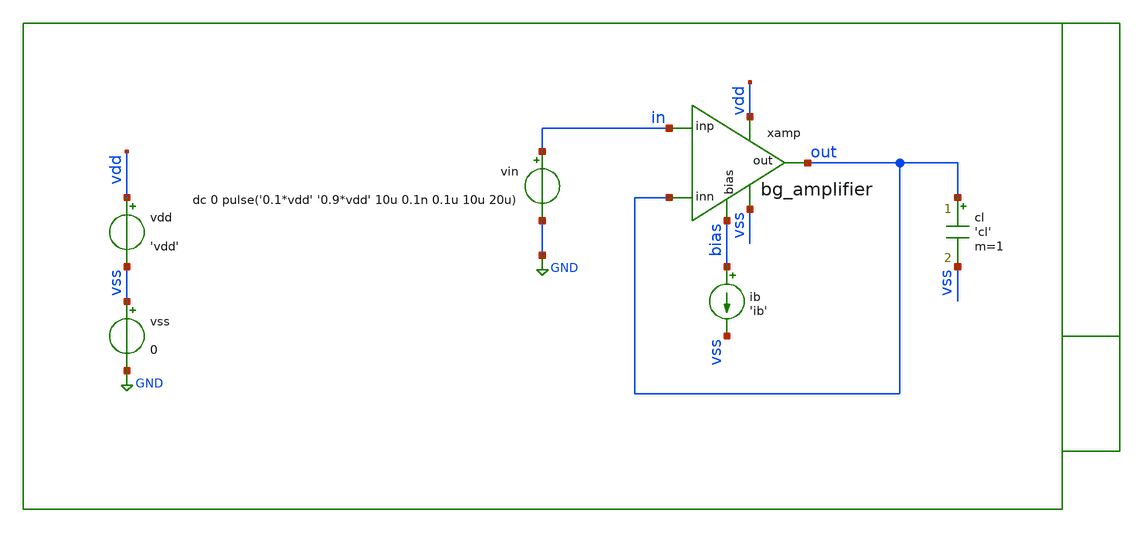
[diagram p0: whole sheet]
** sch_path: xschem/tb/bandgap_cm/bg_amplifier/tr_bg_amplifier_slew.sch
**.subckt tr_bg_amplifier_slew
cl out vss 'cl' m=1
vin in GND dc 0 pulse('0.1*vdd' '0.9*vdd' 10u 0.1n 0.1u 10u 20u)
vdd vdd vss 'vdd'
vss vss GND 0
ib bias vss 'ib'
xamp vdd out in out vss bias bg_amplifier
**** begin user architecture code
 * Control

.param vdd=3.3
.param vcm='vdd/2'
.param ib=1u
.param cl=10p

.control
save all

tran 100n 60u uic

meas tran vsupply find v(vdd) at=1u

let vmeas_max=vsupply/2+0.2
let vmeas_min=vsupply/2-0.2


meas tran td_pos TRIG v(out) VAL=vmeas_min RISE=2 TARG v(out) VAL=vmeas_max RISE=2
meas tran td_neg TRIG v(out) VAL=vmeas_max FALL=2 TARG v(out) VAL=vmeas_min FALL=2

let sr_pos=(vmeas_max-vmeas_min)/td_pos
let sr_neg=(vmeas_max-vmeas_min)/td_neg

print sr_pos
print sr_neg

set wr_singlescale
set wr_vecnames
wrdata data.csv out

.endc

 * Model Corners

.include $::CORNERS/ngspice/tt.spice
*.include $::CORNERS/ngspice/ff.spice
*.include $::CORNERS/ngspice/ss.spice
*.include $::CORNERS/ngspice/sf.spice
*.include $::CORNERS/ngspice/fs.spice

 * extract

* pex
*.include $::DESIGN_PATH/sch/bandgap_cm/bg_amplifier/bg_amplifier.pex.spice

**** end user architecture code
**.ends

* expanding   symbol:  sch/bandgap_cm/bg_amplifier/bg_amplifier.sym # of pins=6
** sym_path: xschem/sch/bandgap_cm/bg_amplifier/bg_amplifier.sym
** sch_path: xschem/sch/bandgap_cm/bg_amplifier/bg_amplifier.sch
.subckt bg_amplifier vdd out inp inn vss bias
*.ipin inn
*.ipin inp
*.opin out
*.iopin bias
*.iopin vdd
*.iopin vss
XMB5 vbn1 vbn1 vss vss nfet_06v0 L=2u W=16u nf=2 ad='int((nf+1)/2) * W/nf * 0.18u' as='int((nf+2)/2) * W/nf * 0.18u'
+ pd='2*int((nf+1)/2) * (W/nf + 0.18u)' ps='2*int((nf+2)/2) * (W/nf + 0.18u)' nrd='0.18u / W' nrs='0.18u / W'
+ sa=0 sb=0 sd=0 m=4 par=4
XMC1 von vbn1 vss vss nfet_06v0 L=2u W=16u nf=2 ad='int((nf+1)/2) * W/nf * 0.18u' as='int((nf+2)/2) * W/nf * 0.18u'
+ pd='2*int((nf+1)/2) * (W/nf + 0.18u)' ps='2*int((nf+2)/2) * (W/nf + 0.18u)' nrd='0.18u / W' nrs='0.18u / W'
+ sa=0 sb=0 sd=0 m=10 par=10
XMC2 vop vbn1 vss vss nfet_06v0 L=2u W=16u nf=2 ad='int((nf+1)/2) * W/nf * 0.18u' as='int((nf+2)/2) * W/nf * 0.18u'
+ pd='2*int((nf+1)/2) * (W/nf + 0.18u)' ps='2*int((nf+2)/2) * (W/nf + 0.18u)' nrd='0.18u / W' nrs='0.18u / W'
+ sa=0 sb=0 sd=0 m=10 par=10
XMC3 mirr vbn2 von vss nfet_06v0 L=2u W=16u nf=2 ad='int((nf+1)/2) * W/nf * 0.18u' as='int((nf+2)/2) * W/nf * 0.18u'
+ pd='2*int((nf+1)/2) * (W/nf + 0.18u)' ps='2*int((nf+2)/2) * (W/nf + 0.18u)' nrd='0.18u / W' nrs='0.18u / W'
+ sa=0 sb=0 sd=0 m=4 par=4
XMC4 out vbn2 vop vss nfet_06v0 L=2u W=16u nf=2 ad='int((nf+1)/2) * W/nf * 0.18u' as='int((nf+2)/2) * W/nf * 0.18u'
+ pd='2*int((nf+1)/2) * (W/nf + 0.18u)' ps='2*int((nf+2)/2) * (W/nf + 0.18u)' nrd='0.18u / W' nrs='0.18u / W'
+ sa=0 sb=0 sd=0 m=4 par=4
XMB3 bias bias vbp1 vdd pfet_06v0 L=2u W=16u nf=2 ad='int((nf+1)/2) * W/nf * 0.18u' as='int((nf+2)/2) * W/nf * 0.18u'
+ pd='2*int((nf+1)/2) * (W/nf + 0.18u)' ps='2*int((nf+2)/2) * (W/nf + 0.18u)' nrd='0.18u / W' nrs='0.18u / W'
+ sa=0 sb=0 sd=0 m=2 par=2
XMB1 vbp1 vbp1 vdd vdd pfet_06v0 L=2u W=16u nf=2 ad='int((nf+1)/2) * W/nf * 0.18u' as='int((nf+2)/2) * W/nf * 0.18u'
+ pd='2*int((nf+1)/2) * (W/nf + 0.18u)' ps='2*int((nf+2)/2) * (W/nf + 0.18u)' nrd='0.18u / W' nrs='0.18u / W'
+ sa=0 sb=0 sd=0 m=4 par=4
XMB2 vbn2 vbp1 vdd vdd pfet_06v0 L=2u W=16u nf=2 ad='int((nf+1)/2) * W/nf * 0.18u' as='int((nf+2)/2) * W/nf * 0.18u'
+ pd='2*int((nf+1)/2) * (W/nf + 0.18u)' ps='2*int((nf+2)/2) * (W/nf + 0.18u)' nrd='0.18u / W' nrs='0.18u / W'
+ sa=0 sb=0 sd=0 m=4 par=4
XMT1 vcm vbp1 vdd vdd pfet_06v0 L=2u W=16u nf=2 ad='int((nf+1)/2) * W/nf * 0.18u' as='int((nf+2)/2) * W/nf * 0.18u'
+ pd='2*int((nf+1)/2) * (W/nf + 0.18u)' ps='2*int((nf+2)/2) * (W/nf + 0.18u)' nrd='0.18u / W' nrs='0.18u / W'
+ sa=0 sb=0 sd=0 m=8 par=8
XMD1 von inp vcm vdd pfet_06v0 L=4u W=16u nf=2 ad='int((nf+1)/2) * W/nf * 0.18u' as='int((nf+2)/2) * W/nf * 0.18u'
+ pd='2*int((nf+1)/2) * (W/nf + 0.18u)' ps='2*int((nf+2)/2) * (W/nf + 0.18u)' nrd='0.18u / W' nrs='0.18u / W'
+ sa=0 sb=0 sd=0 m=4 par=4
XMD2 vop inn vcm vdd pfet_06v0 L=4u W=16u nf=2 ad='int((nf+1)/2) * W/nf * 0.18u' as='int((nf+2)/2) * W/nf * 0.18u'
+ pd='2*int((nf+1)/2) * (W/nf + 0.18u)' ps='2*int((nf+2)/2) * (W/nf + 0.18u)' nrd='0.18u / W' nrs='0.18u / W'
+ sa=0 sb=0 sd=0 m=4 par=4
XMC7 vda mirr vdd vdd pfet_06v0 L=2u W=16u nf=2 ad='int((nf+1)/2) * W/nf * 0.18u' as='int((nf+2)/2) * W/nf * 0.18u'
+ pd='2*int((nf+1)/2) * (W/nf + 0.18u)' ps='2*int((nf+2)/2) * (W/nf + 0.18u)' nrd='0.18u / W' nrs='0.18u / W'
+ sa=0 sb=0 sd=0 m=2 par=2
XMC8 vdb mirr vdd vdd pfet_06v0 L=2u W=16u nf=2 ad='int((nf+1)/2) * W/nf * 0.18u' as='int((nf+2)/2) * W/nf * 0.18u'
+ pd='2*int((nf+1)/2) * (W/nf + 0.18u)' ps='2*int((nf+2)/2) * (W/nf + 0.18u)' nrd='0.18u / W' nrs='0.18u / W'
+ sa=0 sb=0 sd=0 m=2 par=2
XMC5 mirr bias vda vdd pfet_06v0 L=2u W=16u nf=2 ad='int((nf+1)/2) * W/nf * 0.18u' as='int((nf+2)/2) * W/nf * 0.18u'
+ pd='2*int((nf+1)/2) * (W/nf + 0.18u)' ps='2*int((nf+2)/2) * (W/nf + 0.18u)' nrd='0.18u / W' nrs='0.18u / W'
+ sa=0 sb=0 sd=0 m=4 par=4
XMC6 out bias vdb vdd pfet_06v0 L=2u W=16u nf=2 ad='int((nf+1)/2) * W/nf * 0.18u' as='int((nf+2)/2) * W/nf * 0.18u'
+ pd='2*int((nf+1)/2) * (W/nf + 0.18u)' ps='2*int((nf+2)/2) * (W/nf + 0.18u)' nrd='0.18u / W' nrs='0.18u / W'
+ sa=0 sb=0 sd=0 m=4 par=4
XMB4 vbn2 vbn2 vbn1 vss nfet_06v0 L=2u W=16u nf=2 ad='int((nf+1)/2) * W/nf * 0.18u' as='int((nf+2)/2) * W/nf * 0.18u'
+ pd='2*int((nf+1)/2) * (W/nf + 0.18u)' ps='2*int((nf+2)/2) * (W/nf + 0.18u)' nrd='0.18u / W' nrs='0.18u / W'
+ sa=0 sb=0 sd=0 m=4 par=4
XMDUM1 vdd vdd vdd vdd pfet_06v0 L=2u W=16u nf=2 ad='int((nf+1)/2) * W/nf * 0.18u' as='int((nf+2)/2) * W/nf * 0.18u'
+ pd='2*int((nf+1)/2) * (W/nf + 0.18u)' ps='2*int((nf+2)/2) * (W/nf + 0.18u)' nrd='0.18u / W' nrs='0.18u / W'
+ sa=0 sb=0 sd=0 m=4 par=4
XMDUM2 vdd vdd vdd vdd pfet_06v0 L=2u W=16u nf=2 ad='int((nf+1)/2) * W/nf * 0.18u' as='int((nf+2)/2) * W/nf * 0.18u'
+ pd='2*int((nf+1)/2) * (W/nf + 0.18u)' ps='2*int((nf+2)/2) * (W/nf + 0.18u)' nrd='0.18u / W' nrs='0.18u / W'
+ sa=0 sb=0 sd=0 m=4 par=4
XMDUM3 vdd vdd vdd vdd pfet_06v0 L=2u W=16u nf=2 ad='int((nf+1)/2) * W/nf * 0.18u' as='int((nf+2)/2) * W/nf * 0.18u'
+ pd='2*int((nf+1)/2) * (W/nf + 0.18u)' ps='2*int((nf+2)/2) * (W/nf + 0.18u)' nrd='0.18u / W' nrs='0.18u / W'
+ sa=0 sb=0 sd=0 m=2 par=2
XMDUM4 vss vss vss vss nfet_06v0 L=2u W=16u nf=2 ad='int((nf+1)/2) * W/nf * 0.18u' as='int((nf+2)/2) * W/nf * 0.18u'
+ pd='2*int((nf+1)/2) * (W/nf + 0.18u)' ps='2*int((nf+2)/2) * (W/nf + 0.18u)' nrd='0.18u / W' nrs='0.18u / W'
+ sa=0 sb=0 sd=0 m=2 par=2
XMDUM5 vss vss vss vss nfet_06v0 L=2u W=16u nf=2 ad='int((nf+1)/2) * W/nf * 0.18u' as='int((nf+2)/2) * W/nf * 0.18u'
+ pd='2*int((nf+1)/2) * (W/nf + 0.18u)' ps='2*int((nf+2)/2) * (W/nf + 0.18u)' nrd='0.18u / W' nrs='0.18u / W'
+ sa=0 sb=0 sd=0 m=2 par=2
XMDUM6 vdd vdd vdd vdd pfet_06v0 L=4u W=16u nf=2 ad='int((nf+1)/2) * W/nf * 0.18u' as='int((nf+2)/2) * W/nf * 0.18u'
+ pd='2*int((nf+1)/2) * (W/nf + 0.18u)' ps='2*int((nf+2)/2) * (W/nf + 0.18u)' nrd='0.18u / W' nrs='0.18u / W'
+ sa=0 sb=0 sd=0 m=16 par=16
.ends

.GLOBAL GND
.end
